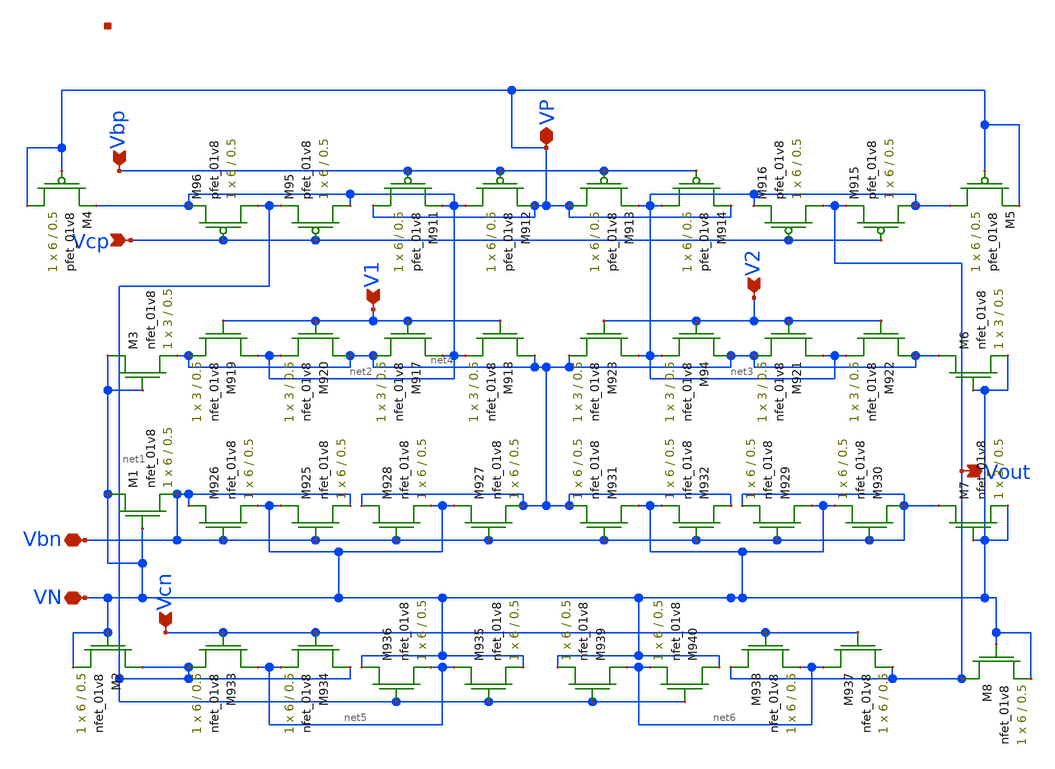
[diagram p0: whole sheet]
** sch_path: mp3/schematic/lds/amp.sch
**.subckt amp VP VN Vout V1 V2 Vbp Vcp Vbn Vcn
*.iopin VP
*.iopin VN
*.opin Vout
*.ipin V1
*.ipin V2
*.ipin Vbp
*.ipin Vcp
*.iopin Vbn
*.ipin Vcn
XM95 net2 Vcp net1 VDD sky130_fd_pr__pfet_01v8 L=0.5 W=6 nf=1 ad='int((nf+1)/2) * W/nf * 0.29' as='int((nf+2)/2) * W/nf * 0.29'
+ pd='2*int((nf+1)/2) * (W/nf + 0.29)' ps='2*int((nf+2)/2) * (W/nf + 0.29)' nrd='0.29 / W' nrs='0.29 / W'
+ sa=0 sb=0 sd=0 mult=1 m=1
XM96 net1 Vcp net2 VDD sky130_fd_pr__pfet_01v8 L=0.5 W=6 nf=1 ad='int((nf+1)/2) * W/nf * 0.29' as='int((nf+2)/2) * W/nf * 0.29'
+ pd='2*int((nf+1)/2) * (W/nf + 0.29)' ps='2*int((nf+2)/2) * (W/nf + 0.29)' nrd='0.29 / W' nrs='0.29 / W'
+ sa=0 sb=0 sd=0 mult=1 m=1
XM911 VP Vbp net2 VDD sky130_fd_pr__pfet_01v8 L=0.5 W=6 nf=1 ad='int((nf+1)/2) * W/nf * 0.29' as='int((nf+2)/2) * W/nf * 0.29'
+ pd='2*int((nf+1)/2) * (W/nf + 0.29)' ps='2*int((nf+2)/2) * (W/nf + 0.29)' nrd='0.29 / W' nrs='0.29 / W'
+ sa=0 sb=0 sd=0 mult=1 m=1
XM912 net2 Vbp VP VDD sky130_fd_pr__pfet_01v8 L=0.5 W=6 nf=1 ad='int((nf+1)/2) * W/nf * 0.29' as='int((nf+2)/2) * W/nf * 0.29'
+ pd='2*int((nf+1)/2) * (W/nf + 0.29)' ps='2*int((nf+2)/2) * (W/nf + 0.29)' nrd='0.29 / W' nrs='0.29 / W'
+ sa=0 sb=0 sd=0 mult=1 m=1
XM913 VP Vbp net3 VDD sky130_fd_pr__pfet_01v8 L=0.5 W=6 nf=1 ad='int((nf+1)/2) * W/nf * 0.29' as='int((nf+2)/2) * W/nf * 0.29'
+ pd='2*int((nf+1)/2) * (W/nf + 0.29)' ps='2*int((nf+2)/2) * (W/nf + 0.29)' nrd='0.29 / W' nrs='0.29 / W'
+ sa=0 sb=0 sd=0 mult=1 m=1
XM914 net3 Vbp VP VDD sky130_fd_pr__pfet_01v8 L=0.5 W=6 nf=1 ad='int((nf+1)/2) * W/nf * 0.29' as='int((nf+2)/2) * W/nf * 0.29'
+ pd='2*int((nf+1)/2) * (W/nf + 0.29)' ps='2*int((nf+2)/2) * (W/nf + 0.29)' nrd='0.29 / W' nrs='0.29 / W'
+ sa=0 sb=0 sd=0 mult=1 m=1
XM915 net3 Vcp Vout VDD sky130_fd_pr__pfet_01v8 L=0.5 W=6 nf=1 ad='int((nf+1)/2) * W/nf * 0.29' as='int((nf+2)/2) * W/nf * 0.29'
+ pd='2*int((nf+1)/2) * (W/nf + 0.29)' ps='2*int((nf+2)/2) * (W/nf + 0.29)' nrd='0.29 / W' nrs='0.29 / W'
+ sa=0 sb=0 sd=0 mult=1 m=1
XM916 Vout Vcp net3 VDD sky130_fd_pr__pfet_01v8 L=0.5 W=6 nf=1 ad='int((nf+1)/2) * W/nf * 0.29' as='int((nf+2)/2) * W/nf * 0.29'
+ pd='2*int((nf+1)/2) * (W/nf + 0.29)' ps='2*int((nf+2)/2) * (W/nf + 0.29)' nrd='0.29 / W' nrs='0.29 / W'
+ sa=0 sb=0 sd=0 mult=1 m=1
XM917 net2 V1 net4 GND sky130_fd_pr__nfet_01v8 L=0.5 W=3 nf=1 ad='int((nf+1)/2) * W/nf * 0.29' as='int((nf+2)/2) * W/nf * 0.29'
+ pd='2*int((nf+1)/2) * (W/nf + 0.29)' ps='2*int((nf+2)/2) * (W/nf + 0.29)' nrd='0.29 / W' nrs='0.29 / W'
+ sa=0 sb=0 sd=0 mult=1 m=1
XM918 net4 V1 net2 GND sky130_fd_pr__nfet_01v8 L=0.5 W=3 nf=1 ad='int((nf+1)/2) * W/nf * 0.29' as='int((nf+2)/2) * W/nf * 0.29'
+ pd='2*int((nf+1)/2) * (W/nf + 0.29)' ps='2*int((nf+2)/2) * (W/nf + 0.29)' nrd='0.29 / W' nrs='0.29 / W'
+ sa=0 sb=0 sd=0 mult=1 m=1
XM919 net2 V1 net4 GND sky130_fd_pr__nfet_01v8 L=0.5 W=3 nf=1 ad='int((nf+1)/2) * W/nf * 0.29' as='int((nf+2)/2) * W/nf * 0.29'
+ pd='2*int((nf+1)/2) * (W/nf + 0.29)' ps='2*int((nf+2)/2) * (W/nf + 0.29)' nrd='0.29 / W' nrs='0.29 / W'
+ sa=0 sb=0 sd=0 mult=1 m=1
XM920 net4 V1 net2 GND sky130_fd_pr__nfet_01v8 L=0.5 W=3 nf=1 ad='int((nf+1)/2) * W/nf * 0.29' as='int((nf+2)/2) * W/nf * 0.29'
+ pd='2*int((nf+1)/2) * (W/nf + 0.29)' ps='2*int((nf+2)/2) * (W/nf + 0.29)' nrd='0.29 / W' nrs='0.29 / W'
+ sa=0 sb=0 sd=0 mult=1 m=1
XM921 net3 V2 net4 GND sky130_fd_pr__nfet_01v8 L=0.5 W=3 nf=1 ad='int((nf+1)/2) * W/nf * 0.29' as='int((nf+2)/2) * W/nf * 0.29'
+ pd='2*int((nf+1)/2) * (W/nf + 0.29)' ps='2*int((nf+2)/2) * (W/nf + 0.29)' nrd='0.29 / W' nrs='0.29 / W'
+ sa=0 sb=0 sd=0 mult=1 m=1
XM922 net4 V2 net3 GND sky130_fd_pr__nfet_01v8 L=0.5 W=3 nf=1 ad='int((nf+1)/2) * W/nf * 0.29' as='int((nf+2)/2) * W/nf * 0.29'
+ pd='2*int((nf+1)/2) * (W/nf + 0.29)' ps='2*int((nf+2)/2) * (W/nf + 0.29)' nrd='0.29 / W' nrs='0.29 / W'
+ sa=0 sb=0 sd=0 mult=1 m=1
XM923 net3 V2 net4 GND sky130_fd_pr__nfet_01v8 L=0.5 W=3 nf=1 ad='int((nf+1)/2) * W/nf * 0.29' as='int((nf+2)/2) * W/nf * 0.29'
+ pd='2*int((nf+1)/2) * (W/nf + 0.29)' ps='2*int((nf+2)/2) * (W/nf + 0.29)' nrd='0.29 / W' nrs='0.29 / W'
+ sa=0 sb=0 sd=0 mult=1 m=1
XM94 net4 V2 net3 GND sky130_fd_pr__nfet_01v8 L=0.5 W=3 nf=1 ad='int((nf+1)/2) * W/nf * 0.29' as='int((nf+2)/2) * W/nf * 0.29'
+ pd='2*int((nf+1)/2) * (W/nf + 0.29)' ps='2*int((nf+2)/2) * (W/nf + 0.29)' nrd='0.29 / W' nrs='0.29 / W'
+ sa=0 sb=0 sd=0 mult=1 m=1
XM925 VN Vbn Vbn GND sky130_fd_pr__nfet_01v8 L=0.5 W=6 nf=1 ad='int((nf+1)/2) * W/nf * 0.29' as='int((nf+2)/2) * W/nf * 0.29'
+ pd='2*int((nf+1)/2) * (W/nf + 0.29)' ps='2*int((nf+2)/2) * (W/nf + 0.29)' nrd='0.29 / W' nrs='0.29 / W'
+ sa=0 sb=0 sd=0 mult=1 m=1
XM926 Vbn Vbn VN GND sky130_fd_pr__nfet_01v8 L=0.5 W=6 nf=1 ad='int((nf+1)/2) * W/nf * 0.29' as='int((nf+2)/2) * W/nf * 0.29'
+ pd='2*int((nf+1)/2) * (W/nf + 0.29)' ps='2*int((nf+2)/2) * (W/nf + 0.29)' nrd='0.29 / W' nrs='0.29 / W'
+ sa=0 sb=0 sd=0 mult=1 m=1
XM927 VN Vbn net4 GND sky130_fd_pr__nfet_01v8 L=0.5 W=6 nf=1 ad='int((nf+1)/2) * W/nf * 0.29' as='int((nf+2)/2) * W/nf * 0.29'
+ pd='2*int((nf+1)/2) * (W/nf + 0.29)' ps='2*int((nf+2)/2) * (W/nf + 0.29)' nrd='0.29 / W' nrs='0.29 / W'
+ sa=0 sb=0 sd=0 mult=1 m=1
XM928 net4 Vbn VN GND sky130_fd_pr__nfet_01v8 L=0.5 W=6 nf=1 ad='int((nf+1)/2) * W/nf * 0.29' as='int((nf+2)/2) * W/nf * 0.29'
+ pd='2*int((nf+1)/2) * (W/nf + 0.29)' ps='2*int((nf+2)/2) * (W/nf + 0.29)' nrd='0.29 / W' nrs='0.29 / W'
+ sa=0 sb=0 sd=0 mult=1 m=1
XM929 VN Vbn Vbn GND sky130_fd_pr__nfet_01v8 L=0.5 W=6 nf=1 ad='int((nf+1)/2) * W/nf * 0.29' as='int((nf+2)/2) * W/nf * 0.29'
+ pd='2*int((nf+1)/2) * (W/nf + 0.29)' ps='2*int((nf+2)/2) * (W/nf + 0.29)' nrd='0.29 / W' nrs='0.29 / W'
+ sa=0 sb=0 sd=0 mult=1 m=1
XM930 Vbn Vbn VN GND sky130_fd_pr__nfet_01v8 L=0.5 W=6 nf=1 ad='int((nf+1)/2) * W/nf * 0.29' as='int((nf+2)/2) * W/nf * 0.29'
+ pd='2*int((nf+1)/2) * (W/nf + 0.29)' ps='2*int((nf+2)/2) * (W/nf + 0.29)' nrd='0.29 / W' nrs='0.29 / W'
+ sa=0 sb=0 sd=0 mult=1 m=1
XM931 VN Vbn net4 GND sky130_fd_pr__nfet_01v8 L=0.5 W=6 nf=1 ad='int((nf+1)/2) * W/nf * 0.29' as='int((nf+2)/2) * W/nf * 0.29'
+ pd='2*int((nf+1)/2) * (W/nf + 0.29)' ps='2*int((nf+2)/2) * (W/nf + 0.29)' nrd='0.29 / W' nrs='0.29 / W'
+ sa=0 sb=0 sd=0 mult=1 m=1
XM932 net4 Vbn VN GND sky130_fd_pr__nfet_01v8 L=0.5 W=6 nf=1 ad='int((nf+1)/2) * W/nf * 0.29' as='int((nf+2)/2) * W/nf * 0.29'
+ pd='2*int((nf+1)/2) * (W/nf + 0.29)' ps='2*int((nf+2)/2) * (W/nf + 0.29)' nrd='0.29 / W' nrs='0.29 / W'
+ sa=0 sb=0 sd=0 mult=1 m=1
XM933 net5 Vcn net1 GND sky130_fd_pr__nfet_01v8 L=0.5 W=6 nf=1 ad='int((nf+1)/2) * W/nf * 0.29' as='int((nf+2)/2) * W/nf * 0.29'
+ pd='2*int((nf+1)/2) * (W/nf + 0.29)' ps='2*int((nf+2)/2) * (W/nf + 0.29)' nrd='0.29 / W' nrs='0.29 / W'
+ sa=0 sb=0 sd=0 mult=1 m=1
XM934 net1 Vcn net5 GND sky130_fd_pr__nfet_01v8 L=0.5 W=6 nf=1 ad='int((nf+1)/2) * W/nf * 0.29' as='int((nf+2)/2) * W/nf * 0.29'
+ pd='2*int((nf+1)/2) * (W/nf + 0.29)' ps='2*int((nf+2)/2) * (W/nf + 0.29)' nrd='0.29 / W' nrs='0.29 / W'
+ sa=0 sb=0 sd=0 mult=1 m=1
XM935 net5 net1 VN GND sky130_fd_pr__nfet_01v8 L=0.5 W=6 nf=1 ad='int((nf+1)/2) * W/nf * 0.29' as='int((nf+2)/2) * W/nf * 0.29'
+ pd='2*int((nf+1)/2) * (W/nf + 0.29)' ps='2*int((nf+2)/2) * (W/nf + 0.29)' nrd='0.29 / W' nrs='0.29 / W'
+ sa=0 sb=0 sd=0 mult=1 m=1
XM936 VN net1 net5 GND sky130_fd_pr__nfet_01v8 L=0.5 W=6 nf=1 ad='int((nf+1)/2) * W/nf * 0.29' as='int((nf+2)/2) * W/nf * 0.29'
+ pd='2*int((nf+1)/2) * (W/nf + 0.29)' ps='2*int((nf+2)/2) * (W/nf + 0.29)' nrd='0.29 / W' nrs='0.29 / W'
+ sa=0 sb=0 sd=0 mult=1 m=1
XM937 net6 Vcn Vout GND sky130_fd_pr__nfet_01v8 L=0.5 W=6 nf=1 ad='int((nf+1)/2) * W/nf * 0.29' as='int((nf+2)/2) * W/nf * 0.29'
+ pd='2*int((nf+1)/2) * (W/nf + 0.29)' ps='2*int((nf+2)/2) * (W/nf + 0.29)' nrd='0.29 / W' nrs='0.29 / W'
+ sa=0 sb=0 sd=0 mult=1 m=1
XM938 Vout Vcn net6 GND sky130_fd_pr__nfet_01v8 L=0.5 W=6 nf=1 ad='int((nf+1)/2) * W/nf * 0.29' as='int((nf+2)/2) * W/nf * 0.29'
+ pd='2*int((nf+1)/2) * (W/nf + 0.29)' ps='2*int((nf+2)/2) * (W/nf + 0.29)' nrd='0.29 / W' nrs='0.29 / W'
+ sa=0 sb=0 sd=0 mult=1 m=1
XM939 net6 net1 VN GND sky130_fd_pr__nfet_01v8 L=0.5 W=6 nf=1 ad='int((nf+1)/2) * W/nf * 0.29' as='int((nf+2)/2) * W/nf * 0.29'
+ pd='2*int((nf+1)/2) * (W/nf + 0.29)' ps='2*int((nf+2)/2) * (W/nf + 0.29)' nrd='0.29 / W' nrs='0.29 / W'
+ sa=0 sb=0 sd=0 mult=1 m=1
XM940 VN net1 net6 GND sky130_fd_pr__nfet_01v8 L=0.5 W=6 nf=1 ad='int((nf+1)/2) * W/nf * 0.29' as='int((nf+2)/2) * W/nf * 0.29'
+ pd='2*int((nf+1)/2) * (W/nf + 0.29)' ps='2*int((nf+2)/2) * (W/nf + 0.29)' nrd='0.29 / W' nrs='0.29 / W'
+ sa=0 sb=0 sd=0 mult=1 m=1
XM1 VN VN Vbn GND sky130_fd_pr__nfet_01v8 L=0.5 W=6 nf=1 ad='int((nf+1)/2) * W/nf * 0.29' as='int((nf+2)/2) * W/nf * 0.29'
+ pd='2*int((nf+1)/2) * (W/nf + 0.29)' ps='2*int((nf+2)/2) * (W/nf + 0.29)' nrd='0.29 / W' nrs='0.29 / W'
+ sa=0 sb=0 sd=0 mult=1 m=1
XM2 net1 VN VN GND sky130_fd_pr__nfet_01v8 L=0.5 W=6 nf=1 ad='int((nf+1)/2) * W/nf * 0.29' as='int((nf+2)/2) * W/nf * 0.29'
+ pd='2*int((nf+1)/2) * (W/nf + 0.29)' ps='2*int((nf+2)/2) * (W/nf + 0.29)' nrd='0.29 / W' nrs='0.29 / W'
+ sa=0 sb=0 sd=0 mult=1 m=1
XM3 VN VN net4 GND sky130_fd_pr__nfet_01v8 L=0.5 W=3 nf=1 ad='int((nf+1)/2) * W/nf * 0.29' as='int((nf+2)/2) * W/nf * 0.29'
+ pd='2*int((nf+1)/2) * (W/nf + 0.29)' ps='2*int((nf+2)/2) * (W/nf + 0.29)' nrd='0.29 / W' nrs='0.29 / W'
+ sa=0 sb=0 sd=0 mult=1 m=1
XM4 VP VP net2 VDD sky130_fd_pr__pfet_01v8 L=0.5 W=6 nf=1 ad='int((nf+1)/2) * W/nf * 0.29' as='int((nf+2)/2) * W/nf * 0.29'
+ pd='2*int((nf+1)/2) * (W/nf + 0.29)' ps='2*int((nf+2)/2) * (W/nf + 0.29)' nrd='0.29 / W' nrs='0.29 / W'
+ sa=0 sb=0 sd=0 mult=1 m=1
XM5 net3 VP VP VDD sky130_fd_pr__pfet_01v8 L=0.5 W=6 nf=1 ad='int((nf+1)/2) * W/nf * 0.29' as='int((nf+2)/2) * W/nf * 0.29'
+ pd='2*int((nf+1)/2) * (W/nf + 0.29)' ps='2*int((nf+2)/2) * (W/nf + 0.29)' nrd='0.29 / W' nrs='0.29 / W'
+ sa=0 sb=0 sd=0 mult=1 m=1
XM6 net4 VN VN GND sky130_fd_pr__nfet_01v8 L=0.5 W=3 nf=1 ad='int((nf+1)/2) * W/nf * 0.29' as='int((nf+2)/2) * W/nf * 0.29'
+ pd='2*int((nf+1)/2) * (W/nf + 0.29)' ps='2*int((nf+2)/2) * (W/nf + 0.29)' nrd='0.29 / W' nrs='0.29 / W'
+ sa=0 sb=0 sd=0 mult=1 m=1
XM7 Vbn VN VN GND sky130_fd_pr__nfet_01v8 L=0.5 W=3 nf=1 ad='int((nf+1)/2) * W/nf * 0.29' as='int((nf+2)/2) * W/nf * 0.29'
+ pd='2*int((nf+1)/2) * (W/nf + 0.29)' ps='2*int((nf+2)/2) * (W/nf + 0.29)' nrd='0.29 / W' nrs='0.29 / W'
+ sa=0 sb=0 sd=0 mult=1 m=1
XM8 Vout VN VN GND sky130_fd_pr__nfet_01v8 L=0.5 W=6 nf=1 ad='int((nf+1)/2) * W/nf * 0.29' as='int((nf+2)/2) * W/nf * 0.29'
+ pd='2*int((nf+1)/2) * (W/nf + 0.29)' ps='2*int((nf+2)/2) * (W/nf + 0.29)' nrd='0.29 / W' nrs='0.29 / W'
+ sa=0 sb=0 sd=0 mult=1 m=1
**.ends
.end
